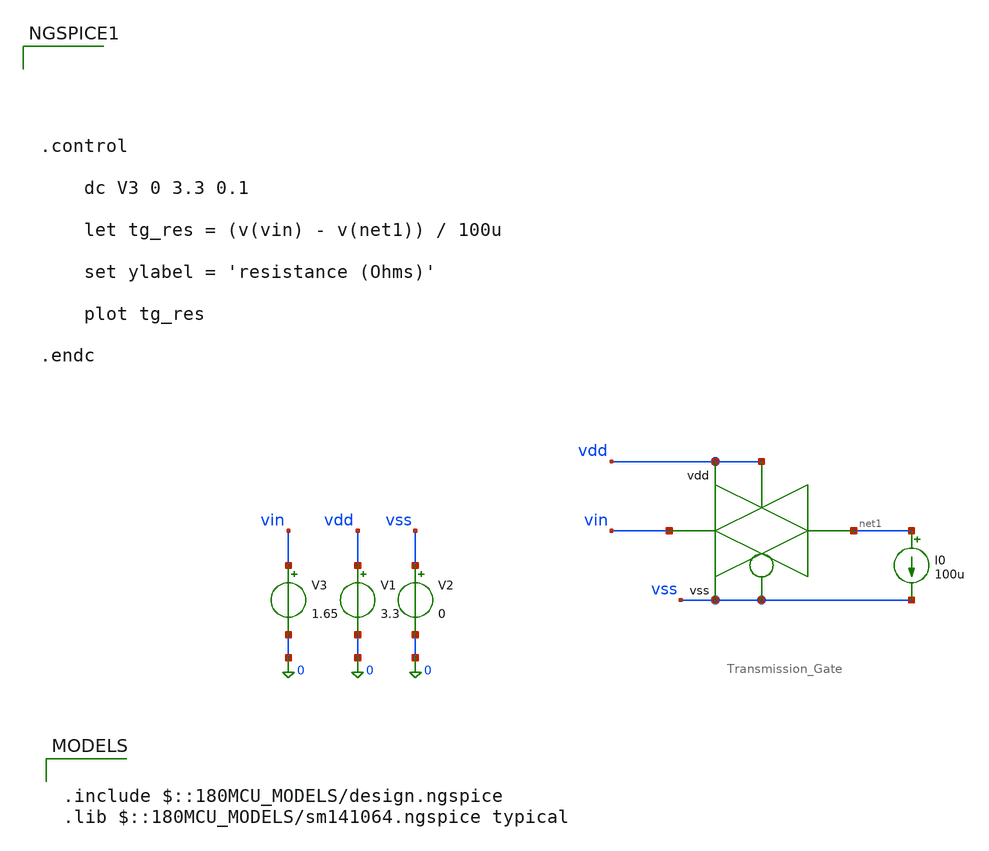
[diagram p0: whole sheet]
** sch_path: simulation/testbench_analog/TG_dynamic-resistance.sch
**.subckt TG_dynamic-resistance
x1 vin vss vdd vdd vss net1 Transmission_Gate
V1 vdd 0 3.3
V2 vss 0 0
V3 vin 0 1.65
I0 net1 vss 100u
**** begin user architecture code





.control

	dc V3 0 3.3 0.1

	let tg_res = (v(vin) - v(net1)) / 100u

	set ylabel = 'resistance (Ohms)'

	plot tg_res

.endc



.include $::180MCU_MODELS/design.ngspice
.lib $::180MCU_MODELS/sm141064.ngspice typical

**** end user architecture code
**.ends

* expanding   symbol:  Transmission_Gate.sym # of pins=6
** sym_path: design/analog/transmission_gate/Transmission_Gate.sym
** sch_path: design/analog/transmission_gate/Transmission_Gate.sch
.subckt Transmission_Gate A en_b en vdd vss B
*.ipin en_b
*.iopin A
*.iopin B
*.ipin en
*.iopin vdd
*.iopin vss
XM1 B en_b A vdd pfet_03v3 L=0.28u W=20u nf=10 ad='int((nf+1)/2) * W/nf * 0.18u' as='int((nf+2)/2) * W/nf * 0.18u'
+ pd='2*int((nf+1)/2) * (W/nf + 0.18u)' ps='2*int((nf+2)/2) * (W/nf + 0.18u)' nrd='0.18u / W' nrs='0.18u / W'
+ sa=0 sb=0 sd=0 m=8
XM2 A en B vss nfet_03v3 L=0.28u W=10u nf=5 ad='int((nf+1)/2) * W/nf * 0.18u' as='int((nf+2)/2) * W/nf * 0.18u'
+ pd='2*int((nf+1)/2) * (W/nf + 0.18u)' ps='2*int((nf+2)/2) * (W/nf + 0.18u)' nrd='0.18u / W' nrs='0.18u / W'
+ sa=0 sb=0 sd=0 m=8
.ends

.end
